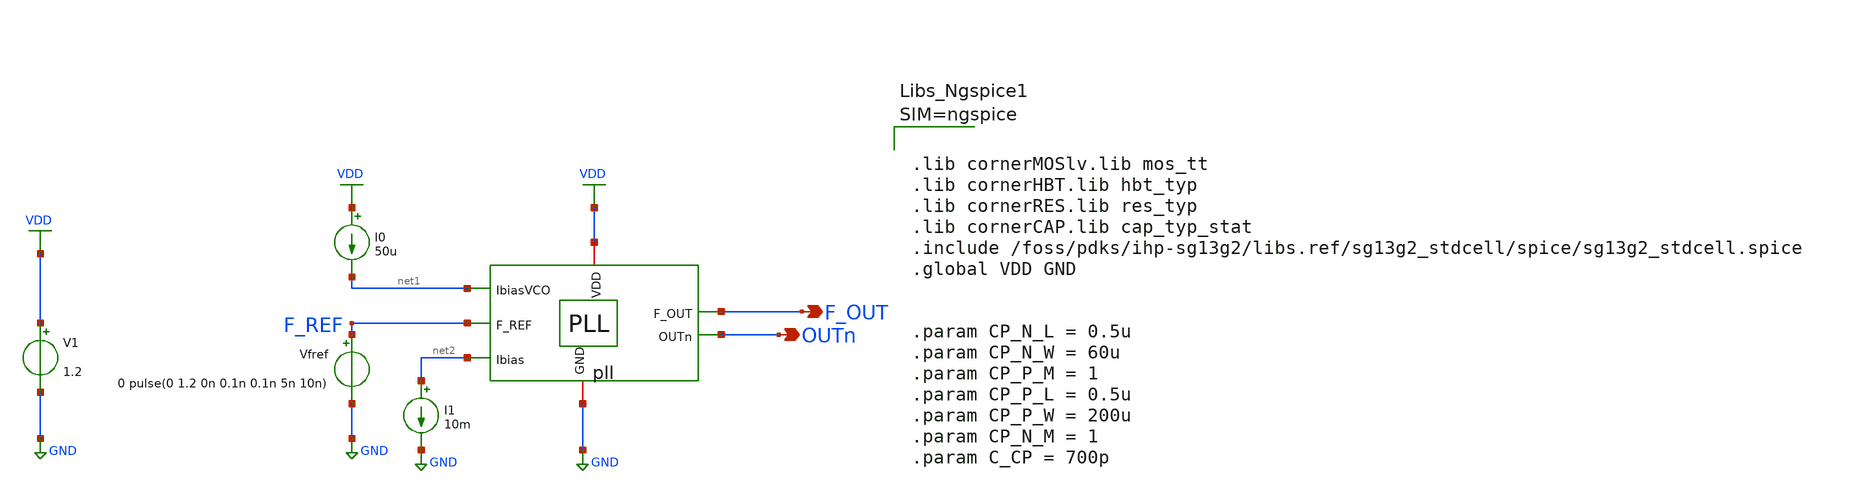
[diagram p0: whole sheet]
** sch_path: schematic/blocks/top-pll/pll_tb.sch
**.subckt pll_tb OUTn F_OUT
*.opin OUTn
*.opin F_OUT
V1 VDD GND 1.2
I0 VDD net1 50u
Vfref F_REF GND 0 pulse(0 1.2 0n 0.1n 0.1n 5n 10n)
I1 net2 GND 10m
x1 F_OUT F_REF net1 OUTn net2 VDD GND pll
**** begin user architecture code



.lib cornerMOSlv.lib mos_tt
.lib cornerHBT.lib hbt_typ
.lib cornerRES.lib res_typ
.lib cornerCAP.lib cap_typ_stat
.include /foss/pdks/ihp-sg13g2/libs.ref/sg13g2_stdcell/spice/sg13g2_stdcell.spice
.global VDD GND


.param CP_N_L = 0.5u
.param CP_N_W = 60u
.param CP_P_M = 1
.param CP_P_L = 0.5u
.param CP_P_W = 200u
.param CP_N_M = 1
.param C_CP = 700p






*****************************************************
* PLL + DSM Frequency Divider Testbench
*****************************************************

.option temp = 27
.param VDD = 1.2

* ==============================
* Include Models
* ==============================

* Inductor / analog models
.include ./IHP_4nH_Inductor.spice

* to generate following file copy stimuli.test
* to the simulation directory and run simulation -> Utile Stimuli Editor (GUI),
* and press 'Translate'
.include stimuli_test.cir

.control

  * Simulation accuracy options
  .options maxstep=10p reltol=1e-4 abstol=1e-9

  * Save important PLL + DSM nodes
  save v(sdata) v(sclk) v(rst) v(dsm_clk) v(F_REF) v(F_OUT) v(vctrl) v(vco_out) v(UP) v(DN)
  set appendwrite

 * Run long enough for PLL lock
  tran 20p 5u uic

  remzerovec

  write pll_dsm_freq_div.raw
.endc



**** end user architecture code
**.ends
.GLOBAL GND
.GLOBAL VDD
.end
